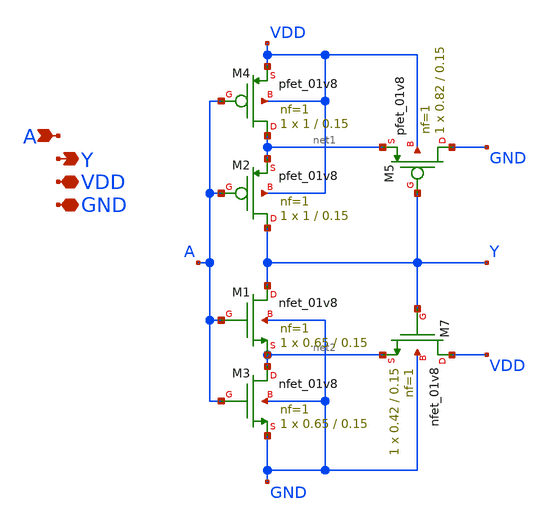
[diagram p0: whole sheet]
** sch_path: design/xschem/schmitt_trigger.sch
**.subckt schmitt_trigger A Y VDD GND
*.ipin A
*.opin Y
*.iopin VDD
*.iopin GND
XM3 net2 A GND GND sky130_fd_pr__nfet_01v8 L=0.15 W=0.65 nf=1 ad='int((nf+1)/2) * W/nf * 0.29' as='int((nf+2)/2) * W/nf * 0.29'
+ pd='2*int((nf+1)/2) * (W/nf + 0.29)' ps='2*int((nf+2)/2) * (W/nf + 0.29)' nrd='0.29 / W' nrs='0.29 / W'
+ sa=0 sb=0 sd=0 mult=1 m=1
XM1 Y A net2 GND sky130_fd_pr__nfet_01v8 L=0.15 W=0.65 nf=1 ad='int((nf+1)/2) * W/nf * 0.29' as='int((nf+2)/2) * W/nf * 0.29'
+ pd='2*int((nf+1)/2) * (W/nf + 0.29)' ps='2*int((nf+2)/2) * (W/nf + 0.29)' nrd='0.29 / W' nrs='0.29 / W'
+ sa=0 sb=0 sd=0 mult=1 m=1
XM7 VDD Y net2 GND sky130_fd_pr__nfet_01v8 L=0.15 W=0.42 nf=1 ad='int((nf+1)/2) * W/nf * 0.29' as='int((nf+2)/2) * W/nf * 0.29'
+ pd='2*int((nf+1)/2) * (W/nf + 0.29)' ps='2*int((nf+2)/2) * (W/nf + 0.29)' nrd='0.29 / W' nrs='0.29 / W'
+ sa=0 sb=0 sd=0 mult=1 m=1
XM4 net1 A VDD VDD sky130_fd_pr__pfet_01v8 L=0.15 W=1 nf=1 ad='int((nf+1)/2) * W/nf * 0.29' as='int((nf+2)/2) * W/nf * 0.29'
+ pd='2*int((nf+1)/2) * (W/nf + 0.29)' ps='2*int((nf+2)/2) * (W/nf + 0.29)' nrd='0.29 / W' nrs='0.29 / W'
+ sa=0 sb=0 sd=0 mult=1 m=1
XM2 Y A net1 VDD sky130_fd_pr__pfet_01v8 L=0.15 W=1 nf=1 ad='int((nf+1)/2) * W/nf * 0.29' as='int((nf+2)/2) * W/nf * 0.29'
+ pd='2*int((nf+1)/2) * (W/nf + 0.29)' ps='2*int((nf+2)/2) * (W/nf + 0.29)' nrd='0.29 / W' nrs='0.29 / W'
+ sa=0 sb=0 sd=0 mult=1 m=1
XM5 GND Y net1 VDD sky130_fd_pr__pfet_01v8 L=0.15 W=0.82 nf=1 ad='int((nf+1)/2) * W/nf * 0.29' as='int((nf+2)/2) * W/nf * 0.29'
+ pd='2*int((nf+1)/2) * (W/nf + 0.29)' ps='2*int((nf+2)/2) * (W/nf + 0.29)' nrd='0.29 / W' nrs='0.29 / W'
+ sa=0 sb=0 sd=0 mult=1 m=1
**.ends
.end
